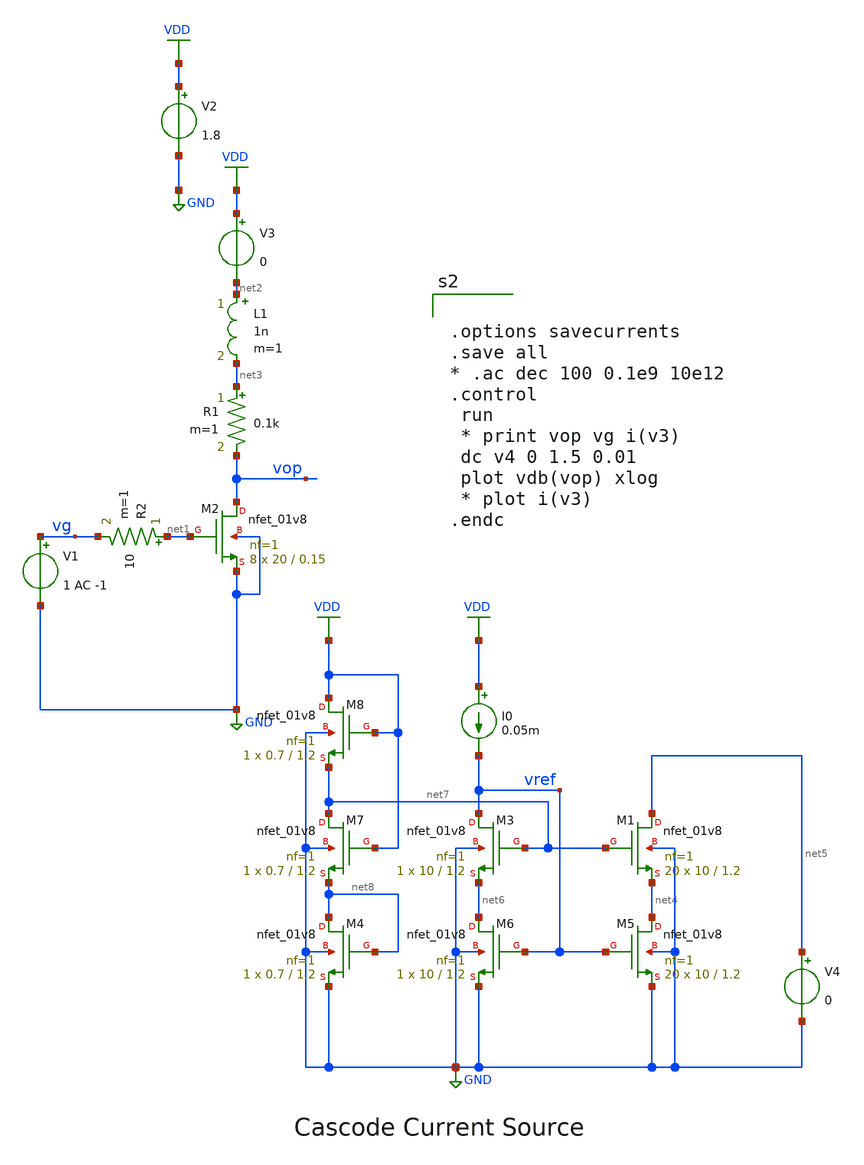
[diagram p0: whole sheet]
** sch_path: xschem/gbp_test.sch
**.subckt gbp_test
V2 VDD GND 1.8
V1 vg GND 1 AC -1
XM2 vop net1 GND GND sky130_fd_pr__nfet_01v8 L=0.15 W=20 nf=1 ad='int((nf+1)/2) * W/nf * 0.29' as='int((nf+2)/2) * W/nf * 0.29'
+ pd='2*int((nf+1)/2) * (W/nf + 0.29)' ps='2*int((nf+2)/2) * (W/nf + 0.29)' nrd='0.29 / W' nrs='0.29 / W'
+ sa=0 sb=0 sd=0 mult=8 m=8
V3 VDD net2 0
R1 net3 vop 0.1k m=1
R2 net1 vg 10 m=1
L1 net2 net3 1n m=1
XM5 net4 vref GND GND sky130_fd_pr__nfet_01v8 L=1.2 W=10 nf=1 ad='int((nf+1)/2) * W/nf * 0.29' as='int((nf+2)/2) * W/nf * 0.29'
+ pd='2*int((nf+1)/2) * (W/nf + 0.29)' ps='2*int((nf+2)/2) * (W/nf + 0.29)' nrd='0.29 / W' nrs='0.29 / W'
+ sa=0 sb=0 sd=0 mult=20 m=20
XM6 net6 vref GND GND sky130_fd_pr__nfet_01v8 L=1.2 W=10 nf=1 ad='int((nf+1)/2) * W/nf * 0.29' as='int((nf+2)/2) * W/nf * 0.29'
+ pd='2*int((nf+1)/2) * (W/nf + 0.29)' ps='2*int((nf+2)/2) * (W/nf + 0.29)' nrd='0.29 / W' nrs='0.29 / W'
+ sa=0 sb=0 sd=0 mult=1 m=1
I0 VDD vref 0.05m
V4 net5 GND 0
XM1 net5 net7 net4 GND sky130_fd_pr__nfet_01v8 L=1.2 W=10 nf=1 ad='int((nf+1)/2) * W/nf * 0.29' as='int((nf+2)/2) * W/nf * 0.29'
+ pd='2*int((nf+1)/2) * (W/nf + 0.29)' ps='2*int((nf+2)/2) * (W/nf + 0.29)' nrd='0.29 / W' nrs='0.29 / W'
+ sa=0 sb=0 sd=0 mult=20 m=20
XM3 vref net7 net6 GND sky130_fd_pr__nfet_01v8 L=1.2 W=10 nf=1 ad='int((nf+1)/2) * W/nf * 0.29' as='int((nf+2)/2) * W/nf * 0.29'
+ pd='2*int((nf+1)/2) * (W/nf + 0.29)' ps='2*int((nf+2)/2) * (W/nf + 0.29)' nrd='0.29 / W' nrs='0.29 / W'
+ sa=0 sb=0 sd=0 mult=1 m=1
XM4 net8 net8 GND GND sky130_fd_pr__nfet_01v8 L=1.2 W=0.7 nf=1 ad='int((nf+1)/2) * W/nf * 0.29' as='int((nf+2)/2) * W/nf * 0.29'
+ pd='2*int((nf+1)/2) * (W/nf + 0.29)' ps='2*int((nf+2)/2) * (W/nf + 0.29)' nrd='0.29 / W' nrs='0.29 / W'
+ sa=0 sb=0 sd=0 mult=1 m=1
XM7 net7 VDD net8 GND sky130_fd_pr__nfet_01v8 L=1.2 W=0.7 nf=1 ad='int((nf+1)/2) * W/nf * 0.29' as='int((nf+2)/2) * W/nf * 0.29'
+ pd='2*int((nf+1)/2) * (W/nf + 0.29)' ps='2*int((nf+2)/2) * (W/nf + 0.29)' nrd='0.29 / W' nrs='0.29 / W'
+ sa=0 sb=0 sd=0 mult=1 m=1
XM8 VDD VDD net7 GND sky130_fd_pr__nfet_01v8 L=1.2 W=0.7 nf=1 ad='int((nf+1)/2) * W/nf * 0.29' as='int((nf+2)/2) * W/nf * 0.29'
+ pd='2*int((nf+1)/2) * (W/nf + 0.29)' ps='2*int((nf+2)/2) * (W/nf + 0.29)' nrd='0.29 / W' nrs='0.29 / W'
+ sa=0 sb=0 sd=0 mult=1 m=1
**** begin user architecture code
.lib $::SKYWATER_MODELS/sky130.lib.spice tt
* .include $::PDKPATH/libs.ref/sky130_fd_sc_hvl/spice/sky130_fd_sc_hvl.spice



.options savecurrents
.save all
* .ac dec 100 0.1e9 10e12
.control
 run
 * print vop vg i(v3)
 dc v4 0 1.5 0.01
 plot vdb(vop) xlog
 * plot i(v3)
.endc


**** end user architecture code
**.ends
.GLOBAL VDD
.GLOBAL GND
.end
